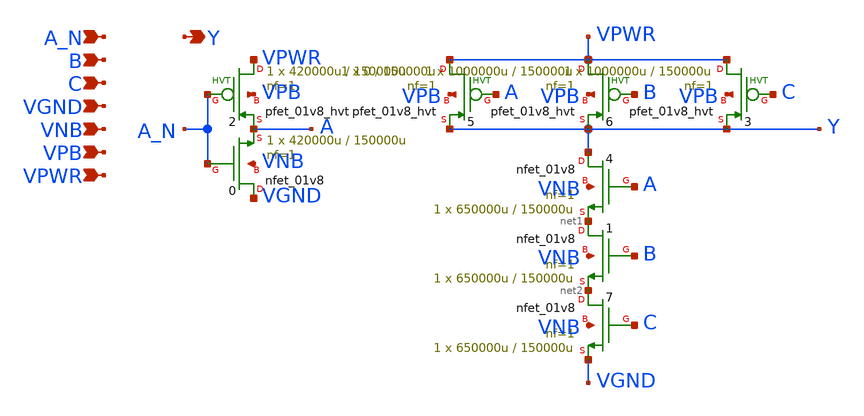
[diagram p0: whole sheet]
** sch_path: schematics/nand3b/sky130_fd_sc_hd__nand3b_1.sch
**.subckt sky130_fd_sc_hd__nand3b_1 A_N B C VGND VNB VPB VPWR Y
*.ipin A_N
*.ipin B
*.ipin C
*.ipin VGND
*.ipin VNB
*.ipin VPB
*.ipin VPWR
*.opin Y
X6 VPWR B Y VPB sky130_fd_pr__pfet_01v8_hvt L=150000u W=1000000u nf=1 ad='int((1 + 1)/2) * 1000000u / 1 * 0.29'
+ as='int((1 + 2)/2) * 1000000u / 1 * 0.29' pd='2*int((1 + 1)/2) * (1000000u / 1 + 0.29)' ps='2*int((1 + 2)/2) * (1000000u / 1 + 0.29)'
+ nrd='0.29 / 1000000u ' nrs='0.29 / 1000000u ' sa=0 sb=0 sd=0 mult=1 m=1
X5 VPWR A Y VPB sky130_fd_pr__pfet_01v8_hvt L=150000u W=0 nf=1 ad='int((1 + 1)/2) * 0 / 1 * 0.29' as='int((1 + 2)/2) * 0 / 1 * 0.29'
+ pd='2*int((1 + 1)/2) * (0 / 1 + 0.29)' ps='2*int((1 + 2)/2) * (0 / 1 + 0.29)' nrd='0.29 / 0 ' nrs='0.29 / 0 '
+ sa=0 sb=0 sd=0 mult=1 m=1
X4 Y A net1 VNB sky130_fd_pr__nfet_01v8 L=150000u W=650000u nf=1 ad='int((1 + 1)/2) * 650000u / 1 * 0.29'
+ as='int((1 + 2)/2) * 650000u / 1 * 0.29' pd='2*int((1 + 1)/2) * (650000u / 1 + 0.29)' ps='2*int((1 + 2)/2) * (650000u / 1 + 0.29)'
+ nrd='0.29 / 650000u ' nrs='0.29 / 650000u ' sa=0 sb=0 sd=0 mult=1 m=1
X1 net1 B net2 VNB sky130_fd_pr__nfet_01v8 L=150000u W=650000u nf=1 ad='int((1 + 1)/2) * 650000u / 1 * 0.29'
+ as='int((1 + 2)/2) * 650000u / 1 * 0.29' pd='2*int((1 + 1)/2) * (650000u / 1 + 0.29)' ps='2*int((1 + 2)/2) * (650000u / 1 + 0.29)'
+ nrd='0.29 / 650000u ' nrs='0.29 / 650000u ' sa=0 sb=0 sd=0 mult=1 m=1
X3 VPWR C Y VPB sky130_fd_pr__pfet_01v8_hvt L=150000u W=1000000u nf=1 ad='int((1 + 1)/2) * 1000000u / 1 * 0.29'
+ as='int((1 + 2)/2) * 1000000u / 1 * 0.29' pd='2*int((1 + 1)/2) * (1000000u / 1 + 0.29)' ps='2*int((1 + 2)/2) * (1000000u / 1 + 0.29)'
+ nrd='0.29 / 1000000u ' nrs='0.29 / 1000000u ' sa=0 sb=0 sd=0 mult=1 m=1
X7 net2 C VGND VNB sky130_fd_pr__nfet_01v8 L=150000u W=650000u nf=1 ad='int((1 + 1)/2) * 650000u / 1 * 0.29'
+ as='int((1 + 2)/2) * 650000u / 1 * 0.29' pd='2*int((1 + 1)/2) * (650000u / 1 + 0.29)' ps='2*int((1 + 2)/2) * (650000u / 1 + 0.29)'
+ nrd='0.29 / 650000u ' nrs='0.29 / 650000u ' sa=0 sb=0 sd=0 mult=1 m=1
X0 VGND A_N A VNB sky130_fd_pr__nfet_01v8 L=150000u W=420000u nf=1 ad='int((1 + 1)/2) * 420000u / 1 * 0.29'
+ as='int((1 + 2)/2) * 420000u / 1 * 0.29' pd='2*int((1 + 1)/2) * (420000u / 1 + 0.29)' ps='2*int((1 + 2)/2) * (420000u / 1 + 0.29)'
+ nrd='0.29 / 420000u ' nrs='0.29 / 420000u ' sa=0 sb=0 sd=0 mult=1 m=1
X2 VPWR A_N A VPB sky130_fd_pr__pfet_01v8_hvt L=150000u W=420000u nf=1 ad='int((1 + 1)/2) * 420000u / 1 * 0.29'
+ as='int((1 + 2)/2) * 420000u / 1 * 0.29' pd='2*int((1 + 1)/2) * (420000u / 1 + 0.29)' ps='2*int((1 + 2)/2) * (420000u / 1 + 0.29)'
+ nrd='0.29 / 420000u ' nrs='0.29 / 420000u ' sa=0 sb=0 sd=0 mult=1 m=1
**.ends
.end
